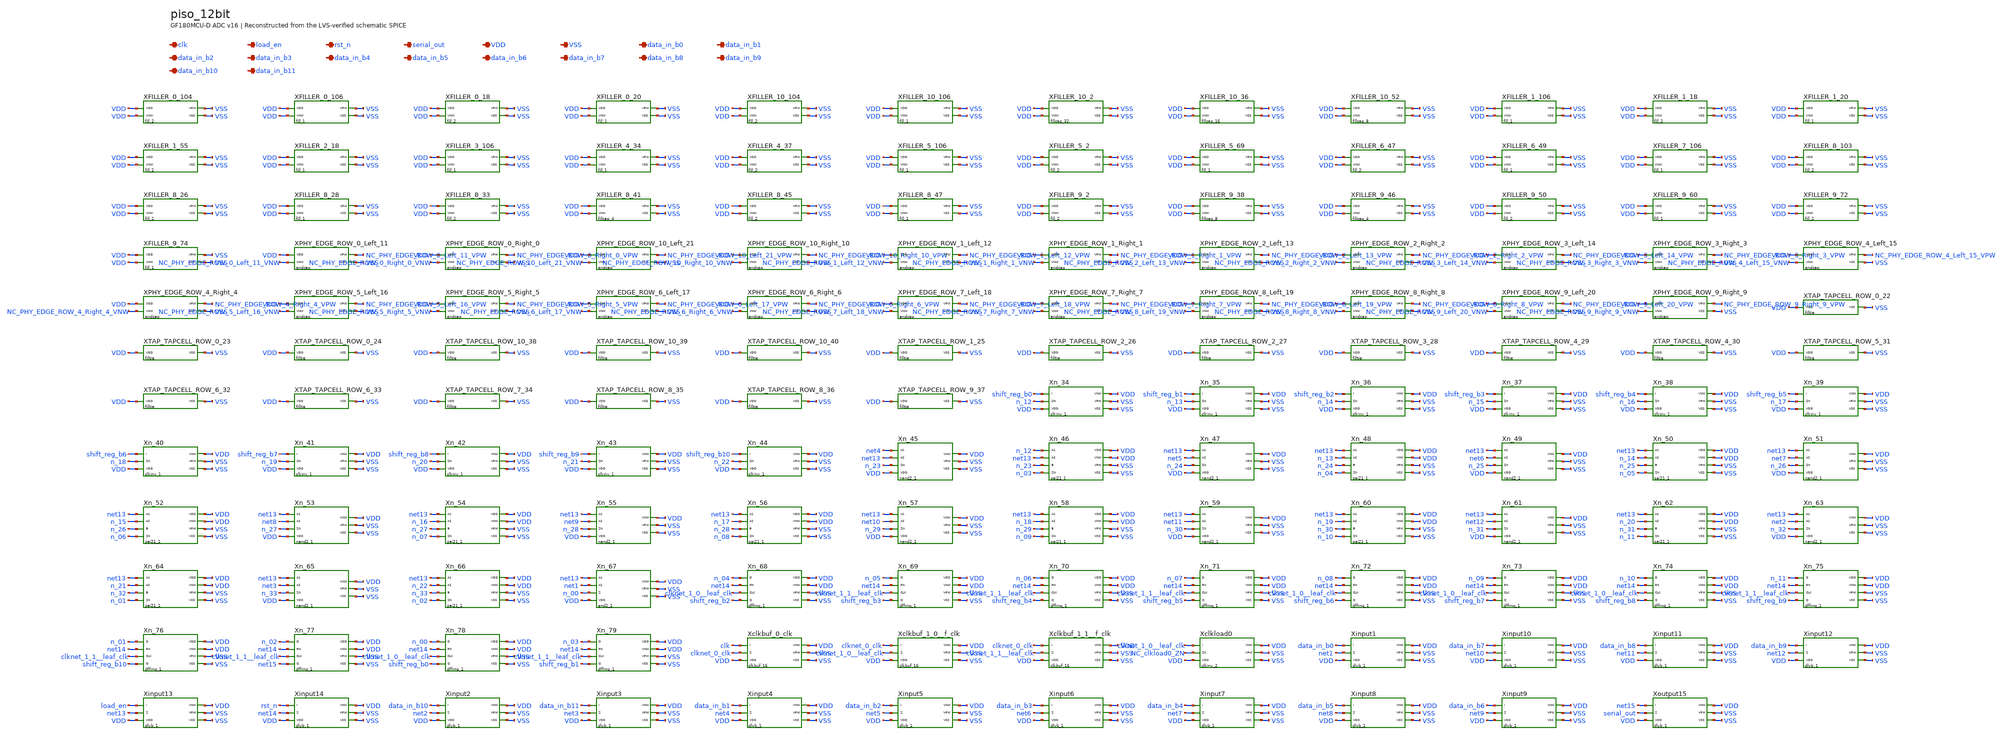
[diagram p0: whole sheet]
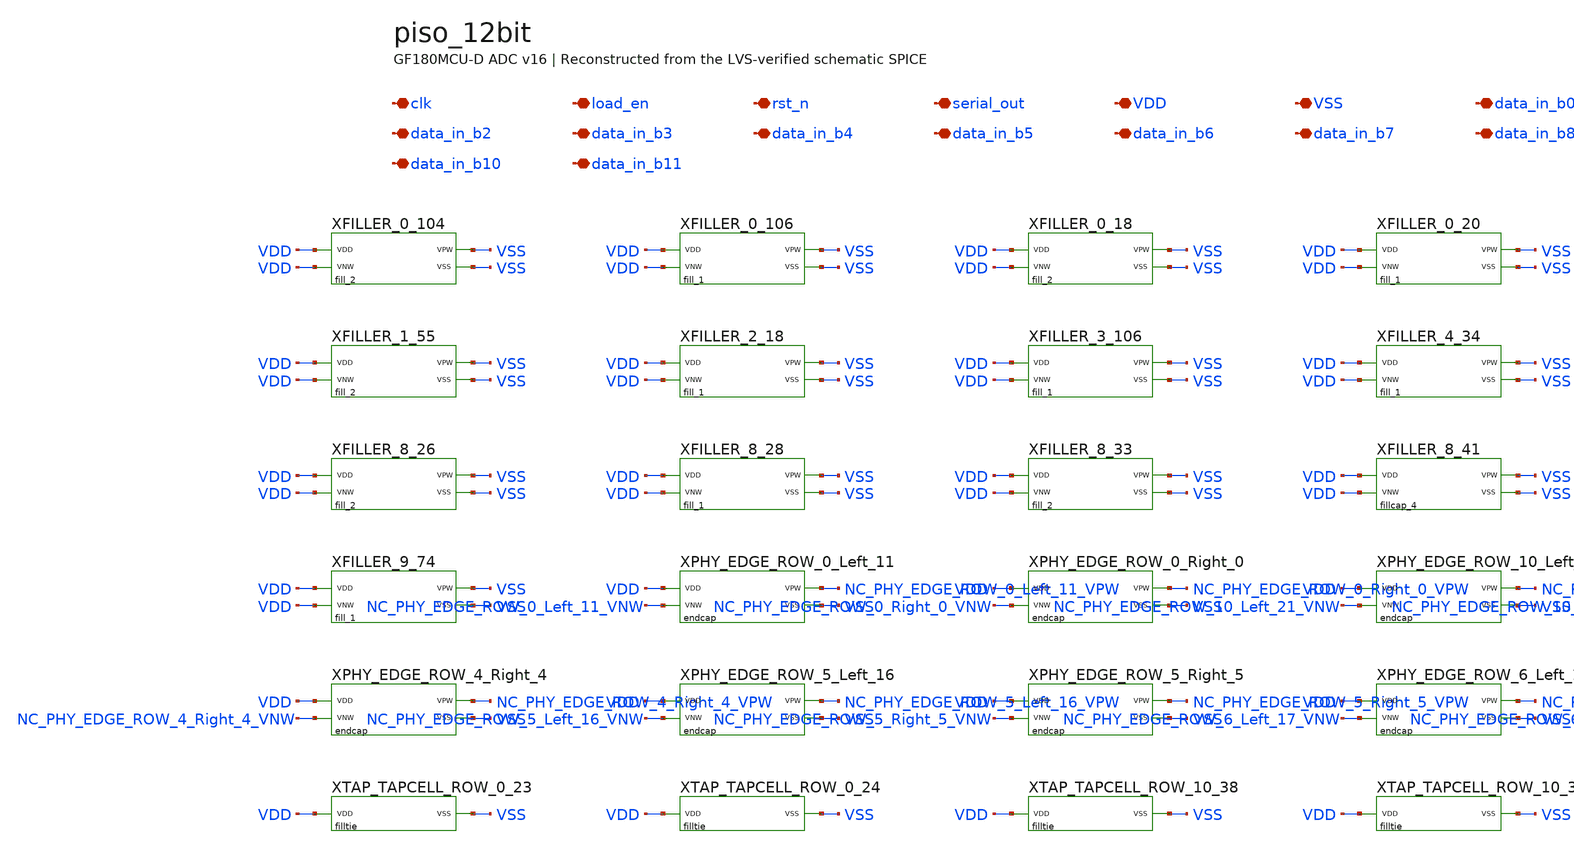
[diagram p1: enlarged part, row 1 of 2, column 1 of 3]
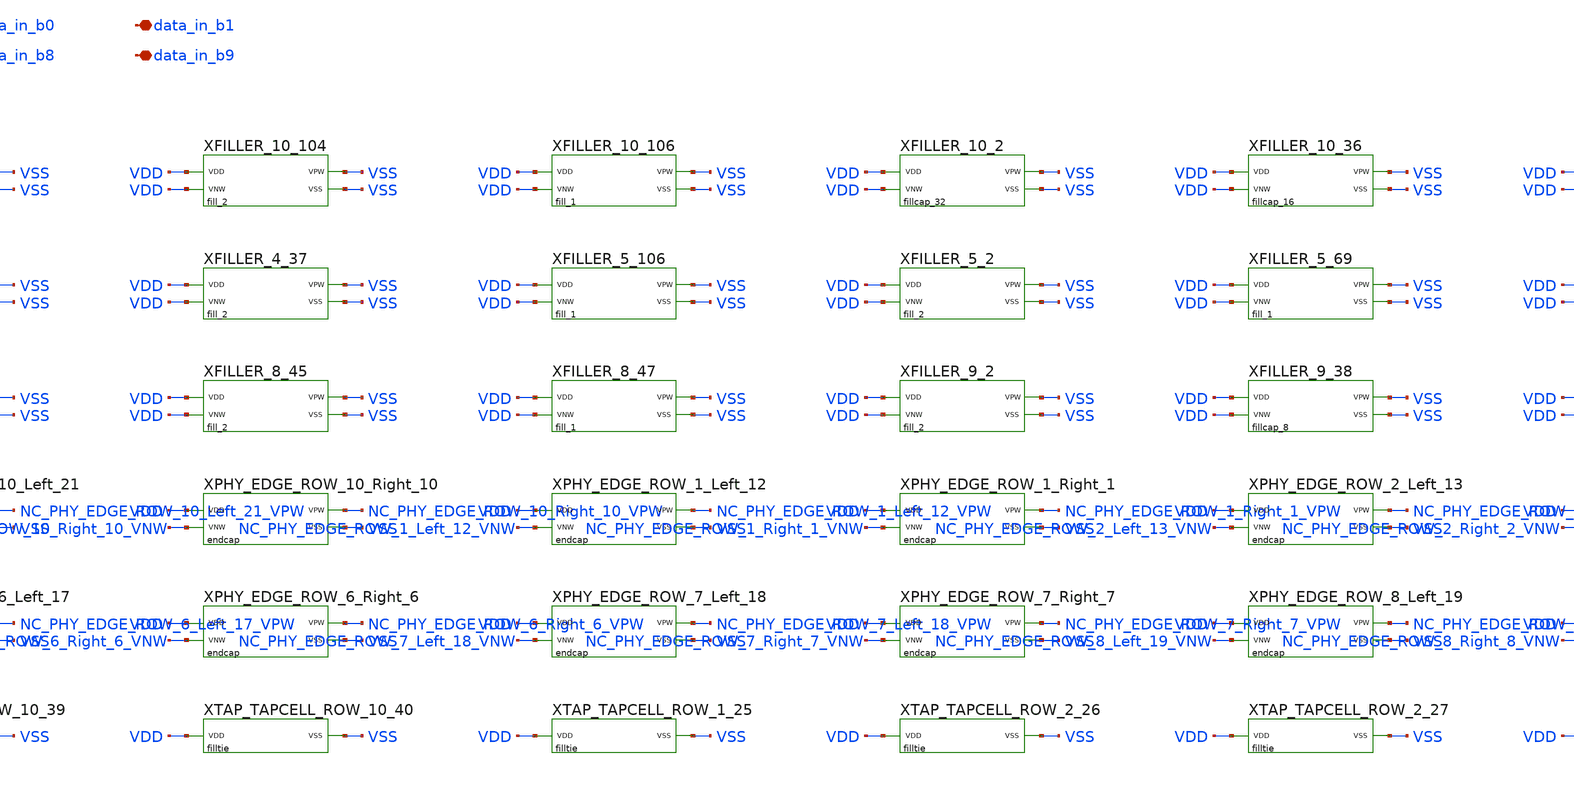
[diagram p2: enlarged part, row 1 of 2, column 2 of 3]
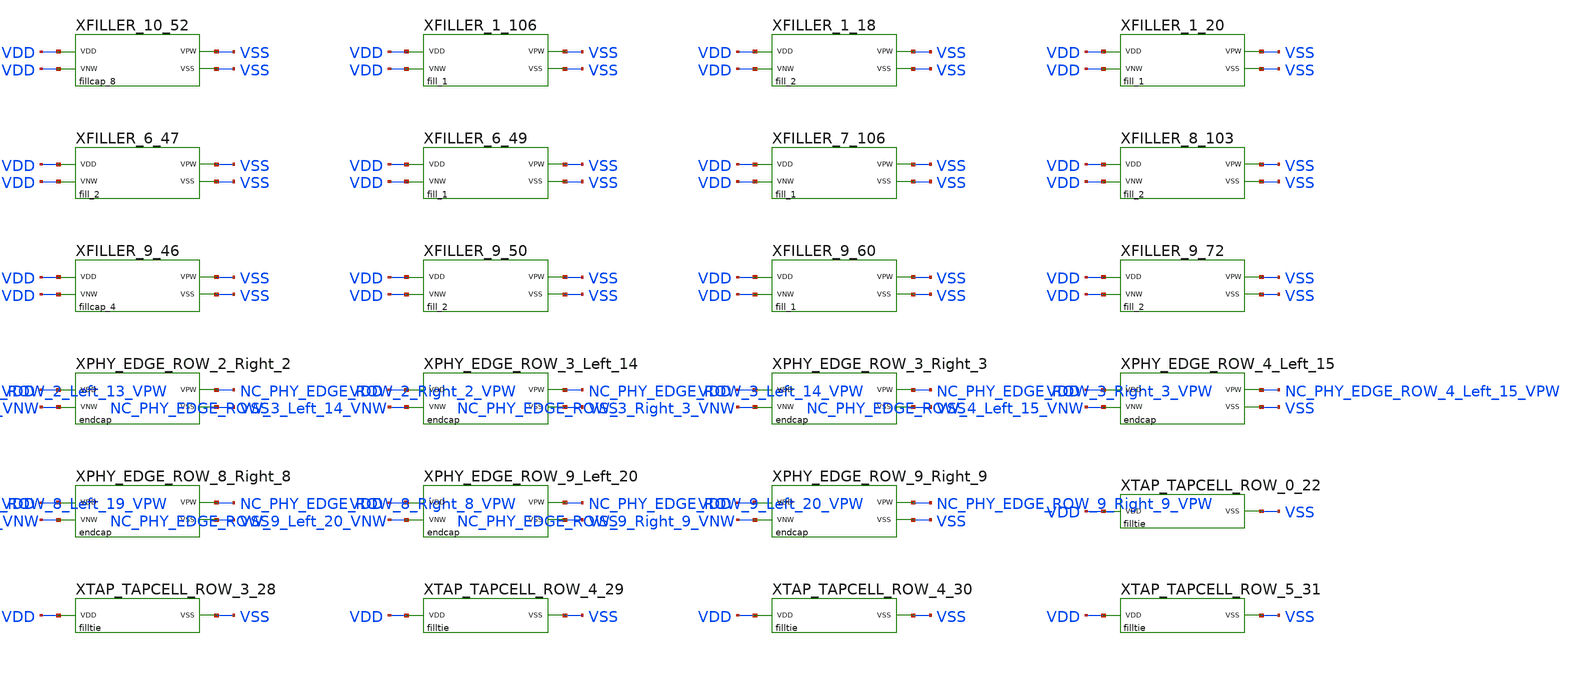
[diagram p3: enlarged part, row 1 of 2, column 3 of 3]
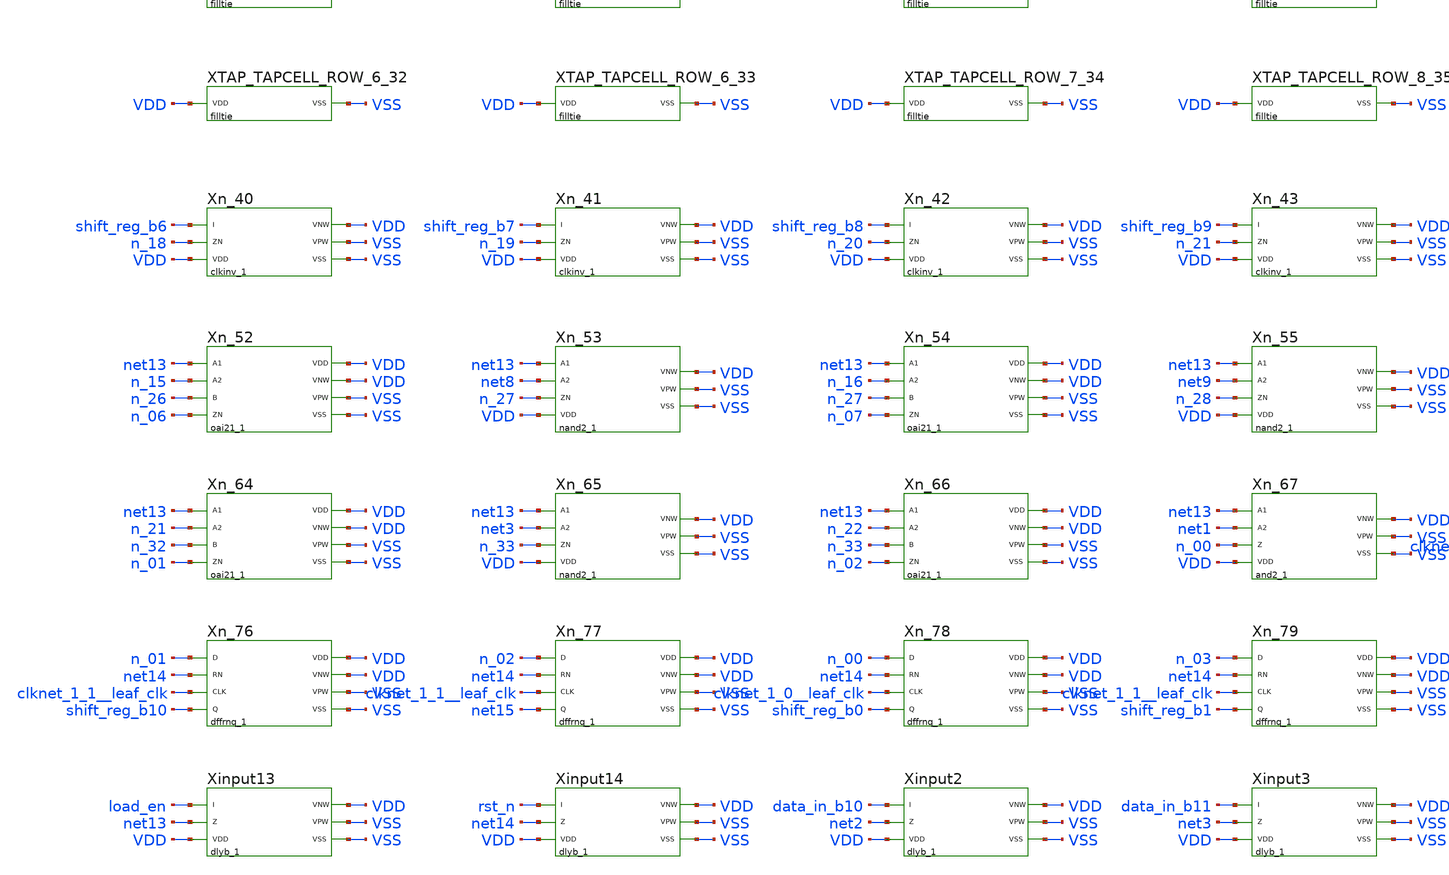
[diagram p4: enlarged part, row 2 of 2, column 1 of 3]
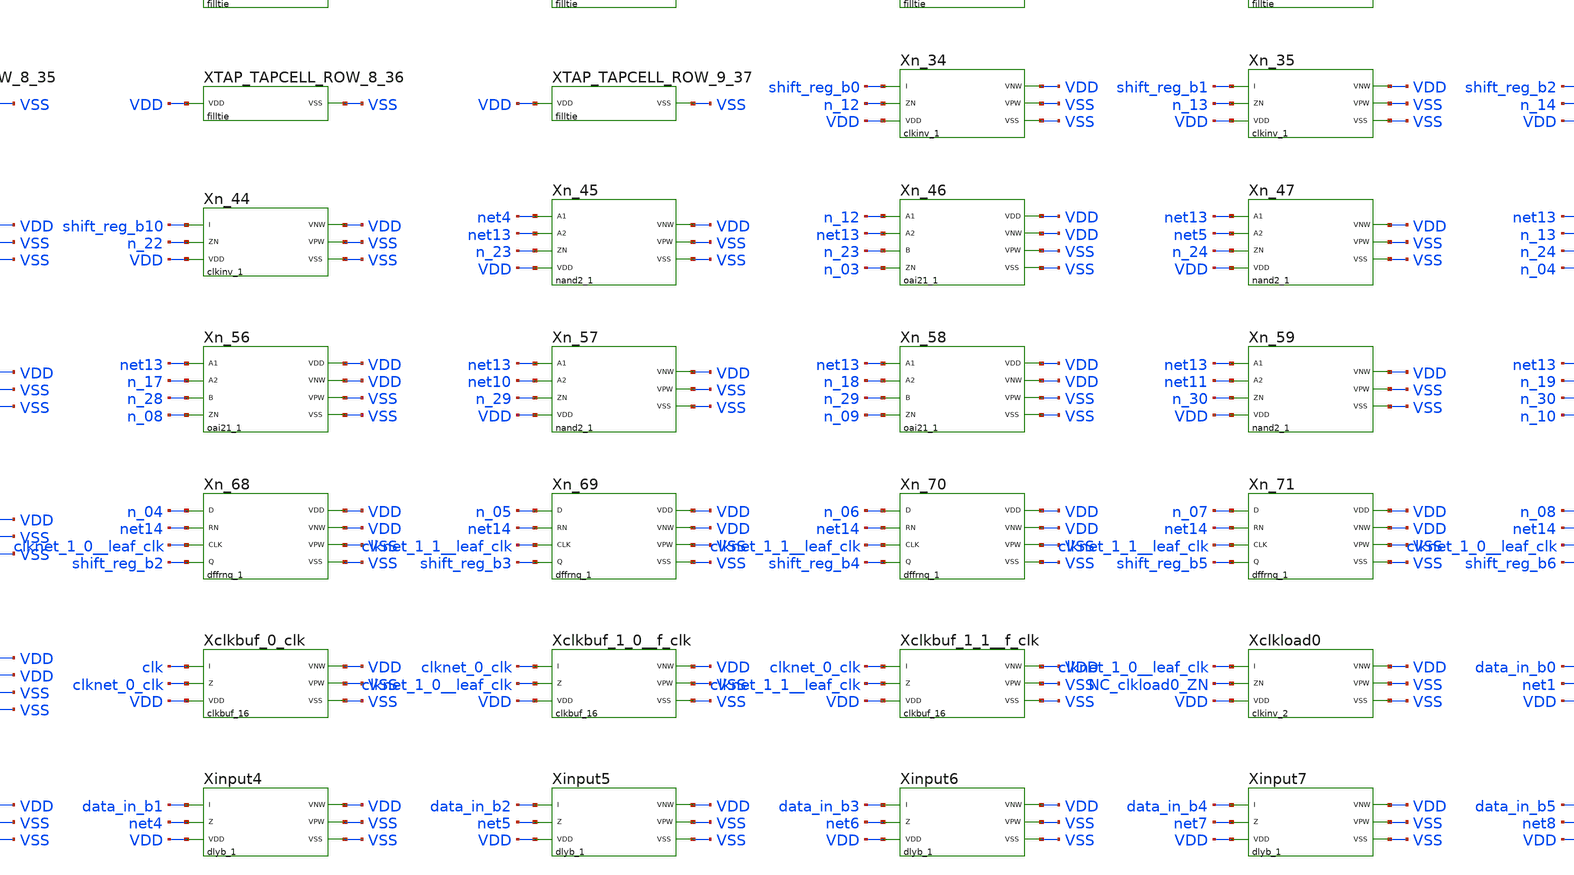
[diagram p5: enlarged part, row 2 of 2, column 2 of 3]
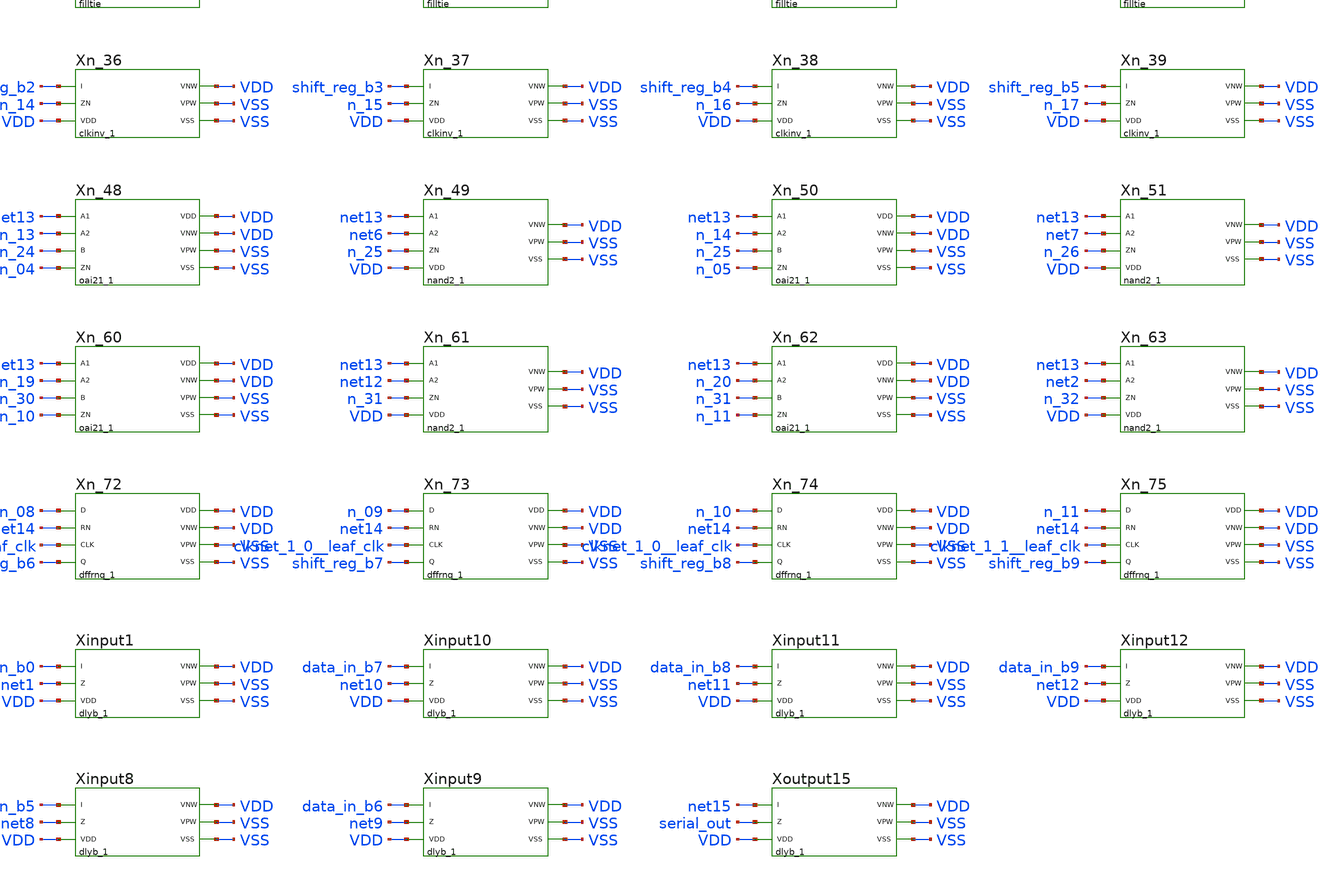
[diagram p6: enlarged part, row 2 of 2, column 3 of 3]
** sch_path: src/schematics/INTEGRATION/ADC_final/ADC_v17_Xschem/piso_12bit.sch
* Copyright (C) 1998-2026 Stefan Frederik Schippers
* This program is free software; you can redistribute it and/or modify
* it under the terms of the GNU General Public License as published by
* the Free Software Foundation; either version 2 of the License, or
* (at your option) any later version.
**.subckt piso_12bit clk load_en rst_n serial_out VDD VSS data_in_b0 data_in_b1 data_in_b2
*+ data_in_b3 data_in_b4 data_in_b5 data_in_b6 data_in_b7 data_in_b8 data_in_b9 data_in_b10 data_in_b11
*.iopin clk
*.iopin load_en
*.iopin rst_n
*.iopin serial_out
*.iopin VDD
*.iopin VSS
*.iopin data_in_b0
*.iopin data_in_b1
*.iopin data_in_b2
*.iopin data_in_b3
*.iopin data_in_b4
*.iopin data_in_b5
*.iopin data_in_b6
*.iopin data_in_b7
*.iopin data_in_b8
*.iopin data_in_b9
*.iopin data_in_b10
*.iopin data_in_b11
XFILLER_0_104 VDD VDD VSS VSS gf180mcu_fd_sc_mcu7t5v0__fill_2
XFILLER_0_106 VDD VDD VSS VSS gf180mcu_fd_sc_mcu7t5v0__fill_1
XFILLER_0_18 VDD VDD VSS VSS gf180mcu_fd_sc_mcu7t5v0__fill_2
XFILLER_0_20 VDD VDD VSS VSS gf180mcu_fd_sc_mcu7t5v0__fill_1
XFILLER_10_104 VDD VDD VSS VSS gf180mcu_fd_sc_mcu7t5v0__fill_2
XFILLER_10_106 VDD VDD VSS VSS gf180mcu_fd_sc_mcu7t5v0__fill_1
XFILLER_10_2 VDD VDD VSS VSS gf180mcu_fd_sc_mcu7t5v0__fillcap_32
XFILLER_10_36 VDD VDD VSS VSS gf180mcu_fd_sc_mcu7t5v0__fillcap_16
XFILLER_10_52 VDD VDD VSS VSS gf180mcu_fd_sc_mcu7t5v0__fillcap_8
XFILLER_1_106 VDD VDD VSS VSS gf180mcu_fd_sc_mcu7t5v0__fill_1
XFILLER_1_18 VDD VDD VSS VSS gf180mcu_fd_sc_mcu7t5v0__fill_2
XFILLER_1_20 VDD VDD VSS VSS gf180mcu_fd_sc_mcu7t5v0__fill_1
XFILLER_1_55 VDD VDD VSS VSS gf180mcu_fd_sc_mcu7t5v0__fill_2
XFILLER_2_18 VDD VDD VSS VSS gf180mcu_fd_sc_mcu7t5v0__fill_1
XFILLER_3_106 VDD VDD VSS VSS gf180mcu_fd_sc_mcu7t5v0__fill_1
XFILLER_4_34 VDD VDD VSS VSS gf180mcu_fd_sc_mcu7t5v0__fill_1
XFILLER_4_37 VDD VDD VSS VSS gf180mcu_fd_sc_mcu7t5v0__fill_2
XFILLER_5_106 VDD VDD VSS VSS gf180mcu_fd_sc_mcu7t5v0__fill_1
XFILLER_5_2 VDD VDD VSS VSS gf180mcu_fd_sc_mcu7t5v0__fill_2
XFILLER_5_69 VDD VDD VSS VSS gf180mcu_fd_sc_mcu7t5v0__fill_1
XFILLER_6_47 VDD VDD VSS VSS gf180mcu_fd_sc_mcu7t5v0__fill_2
XFILLER_6_49 VDD VDD VSS VSS gf180mcu_fd_sc_mcu7t5v0__fill_1
XFILLER_7_106 VDD VDD VSS VSS gf180mcu_fd_sc_mcu7t5v0__fill_1
XFILLER_8_103 VDD VDD VSS VSS gf180mcu_fd_sc_mcu7t5v0__fill_2
XFILLER_8_26 VDD VDD VSS VSS gf180mcu_fd_sc_mcu7t5v0__fill_2
XFILLER_8_28 VDD VDD VSS VSS gf180mcu_fd_sc_mcu7t5v0__fill_1
XFILLER_8_33 VDD VDD VSS VSS gf180mcu_fd_sc_mcu7t5v0__fill_2
XFILLER_8_41 VDD VDD VSS VSS gf180mcu_fd_sc_mcu7t5v0__fillcap_4
XFILLER_8_45 VDD VDD VSS VSS gf180mcu_fd_sc_mcu7t5v0__fill_2
XFILLER_8_47 VDD VDD VSS VSS gf180mcu_fd_sc_mcu7t5v0__fill_1
XFILLER_9_2 VDD VDD VSS VSS gf180mcu_fd_sc_mcu7t5v0__fill_2
XFILLER_9_38 VDD VDD VSS VSS gf180mcu_fd_sc_mcu7t5v0__fillcap_8
XFILLER_9_46 VDD VDD VSS VSS gf180mcu_fd_sc_mcu7t5v0__fillcap_4
XFILLER_9_50 VDD VDD VSS VSS gf180mcu_fd_sc_mcu7t5v0__fill_2
XFILLER_9_60 VDD VDD VSS VSS gf180mcu_fd_sc_mcu7t5v0__fill_1
XFILLER_9_72 VDD VDD VSS VSS gf180mcu_fd_sc_mcu7t5v0__fill_2
XFILLER_9_74 VDD VDD VSS VSS gf180mcu_fd_sc_mcu7t5v0__fill_1
XPHY_EDGE_ROW_0_Left_11 VDD NC_PHY_EDGE_ROW_0_Left_11_VNW NC_PHY_EDGE_ROW_0_Left_11_VPW VSS
+ gf180mcu_fd_sc_mcu7t5v0__endcap
XPHY_EDGE_ROW_0_Right_0 VDD NC_PHY_EDGE_ROW_0_Right_0_VNW NC_PHY_EDGE_ROW_0_Right_0_VPW VSS
+ gf180mcu_fd_sc_mcu7t5v0__endcap
XPHY_EDGE_ROW_10_Left_21 VDD NC_PHY_EDGE_ROW_10_Left_21_VNW NC_PHY_EDGE_ROW_10_Left_21_VPW VSS
+ gf180mcu_fd_sc_mcu7t5v0__endcap
XPHY_EDGE_ROW_10_Right_10 VDD NC_PHY_EDGE_ROW_10_Right_10_VNW NC_PHY_EDGE_ROW_10_Right_10_VPW VSS
+ gf180mcu_fd_sc_mcu7t5v0__endcap
XPHY_EDGE_ROW_1_Left_12 VDD NC_PHY_EDGE_ROW_1_Left_12_VNW NC_PHY_EDGE_ROW_1_Left_12_VPW VSS
+ gf180mcu_fd_sc_mcu7t5v0__endcap
XPHY_EDGE_ROW_1_Right_1 VDD NC_PHY_EDGE_ROW_1_Right_1_VNW NC_PHY_EDGE_ROW_1_Right_1_VPW VSS
+ gf180mcu_fd_sc_mcu7t5v0__endcap
XPHY_EDGE_ROW_2_Left_13 VDD NC_PHY_EDGE_ROW_2_Left_13_VNW NC_PHY_EDGE_ROW_2_Left_13_VPW VSS
+ gf180mcu_fd_sc_mcu7t5v0__endcap
XPHY_EDGE_ROW_2_Right_2 VDD NC_PHY_EDGE_ROW_2_Right_2_VNW NC_PHY_EDGE_ROW_2_Right_2_VPW VSS
+ gf180mcu_fd_sc_mcu7t5v0__endcap
XPHY_EDGE_ROW_3_Left_14 VDD NC_PHY_EDGE_ROW_3_Left_14_VNW NC_PHY_EDGE_ROW_3_Left_14_VPW VSS
+ gf180mcu_fd_sc_mcu7t5v0__endcap
XPHY_EDGE_ROW_3_Right_3 VDD NC_PHY_EDGE_ROW_3_Right_3_VNW NC_PHY_EDGE_ROW_3_Right_3_VPW VSS
+ gf180mcu_fd_sc_mcu7t5v0__endcap
XPHY_EDGE_ROW_4_Left_15 VDD NC_PHY_EDGE_ROW_4_Left_15_VNW NC_PHY_EDGE_ROW_4_Left_15_VPW VSS
+ gf180mcu_fd_sc_mcu7t5v0__endcap
XPHY_EDGE_ROW_4_Right_4 VDD NC_PHY_EDGE_ROW_4_Right_4_VNW NC_PHY_EDGE_ROW_4_Right_4_VPW VSS
+ gf180mcu_fd_sc_mcu7t5v0__endcap
XPHY_EDGE_ROW_5_Left_16 VDD NC_PHY_EDGE_ROW_5_Left_16_VNW NC_PHY_EDGE_ROW_5_Left_16_VPW VSS
+ gf180mcu_fd_sc_mcu7t5v0__endcap
XPHY_EDGE_ROW_5_Right_5 VDD NC_PHY_EDGE_ROW_5_Right_5_VNW NC_PHY_EDGE_ROW_5_Right_5_VPW VSS
+ gf180mcu_fd_sc_mcu7t5v0__endcap
XPHY_EDGE_ROW_6_Left_17 VDD NC_PHY_EDGE_ROW_6_Left_17_VNW NC_PHY_EDGE_ROW_6_Left_17_VPW VSS
+ gf180mcu_fd_sc_mcu7t5v0__endcap
XPHY_EDGE_ROW_6_Right_6 VDD NC_PHY_EDGE_ROW_6_Right_6_VNW NC_PHY_EDGE_ROW_6_Right_6_VPW VSS
+ gf180mcu_fd_sc_mcu7t5v0__endcap
XPHY_EDGE_ROW_7_Left_18 VDD NC_PHY_EDGE_ROW_7_Left_18_VNW NC_PHY_EDGE_ROW_7_Left_18_VPW VSS
+ gf180mcu_fd_sc_mcu7t5v0__endcap
XPHY_EDGE_ROW_7_Right_7 VDD NC_PHY_EDGE_ROW_7_Right_7_VNW NC_PHY_EDGE_ROW_7_Right_7_VPW VSS
+ gf180mcu_fd_sc_mcu7t5v0__endcap
XPHY_EDGE_ROW_8_Left_19 VDD NC_PHY_EDGE_ROW_8_Left_19_VNW NC_PHY_EDGE_ROW_8_Left_19_VPW VSS
+ gf180mcu_fd_sc_mcu7t5v0__endcap
XPHY_EDGE_ROW_8_Right_8 VDD NC_PHY_EDGE_ROW_8_Right_8_VNW NC_PHY_EDGE_ROW_8_Right_8_VPW VSS
+ gf180mcu_fd_sc_mcu7t5v0__endcap
XPHY_EDGE_ROW_9_Left_20 VDD NC_PHY_EDGE_ROW_9_Left_20_VNW NC_PHY_EDGE_ROW_9_Left_20_VPW VSS
+ gf180mcu_fd_sc_mcu7t5v0__endcap
XPHY_EDGE_ROW_9_Right_9 VDD NC_PHY_EDGE_ROW_9_Right_9_VNW NC_PHY_EDGE_ROW_9_Right_9_VPW VSS
+ gf180mcu_fd_sc_mcu7t5v0__endcap
XTAP_TAPCELL_ROW_0_22 VDD VSS gf180mcu_fd_sc_mcu7t5v0__filltie
XTAP_TAPCELL_ROW_0_23 VDD VSS gf180mcu_fd_sc_mcu7t5v0__filltie
XTAP_TAPCELL_ROW_0_24 VDD VSS gf180mcu_fd_sc_mcu7t5v0__filltie
XTAP_TAPCELL_ROW_10_38 VDD VSS gf180mcu_fd_sc_mcu7t5v0__filltie
XTAP_TAPCELL_ROW_10_39 VDD VSS gf180mcu_fd_sc_mcu7t5v0__filltie
XTAP_TAPCELL_ROW_10_40 VDD VSS gf180mcu_fd_sc_mcu7t5v0__filltie
XTAP_TAPCELL_ROW_1_25 VDD VSS gf180mcu_fd_sc_mcu7t5v0__filltie
XTAP_TAPCELL_ROW_2_26 VDD VSS gf180mcu_fd_sc_mcu7t5v0__filltie
XTAP_TAPCELL_ROW_2_27 VDD VSS gf180mcu_fd_sc_mcu7t5v0__filltie
XTAP_TAPCELL_ROW_3_28 VDD VSS gf180mcu_fd_sc_mcu7t5v0__filltie
XTAP_TAPCELL_ROW_4_29 VDD VSS gf180mcu_fd_sc_mcu7t5v0__filltie
XTAP_TAPCELL_ROW_4_30 VDD VSS gf180mcu_fd_sc_mcu7t5v0__filltie
XTAP_TAPCELL_ROW_5_31 VDD VSS gf180mcu_fd_sc_mcu7t5v0__filltie
XTAP_TAPCELL_ROW_6_32 VDD VSS gf180mcu_fd_sc_mcu7t5v0__filltie
XTAP_TAPCELL_ROW_6_33 VDD VSS gf180mcu_fd_sc_mcu7t5v0__filltie
XTAP_TAPCELL_ROW_7_34 VDD VSS gf180mcu_fd_sc_mcu7t5v0__filltie
XTAP_TAPCELL_ROW_8_35 VDD VSS gf180mcu_fd_sc_mcu7t5v0__filltie
XTAP_TAPCELL_ROW_8_36 VDD VSS gf180mcu_fd_sc_mcu7t5v0__filltie
XTAP_TAPCELL_ROW_9_37 VDD VSS gf180mcu_fd_sc_mcu7t5v0__filltie
Xn_34 shift_reg_b0 n_12 VDD VDD VSS VSS gf180mcu_fd_sc_mcu7t5v0__clkinv_1
Xn_35 shift_reg_b1 n_13 VDD VDD VSS VSS gf180mcu_fd_sc_mcu7t5v0__clkinv_1
Xn_36 shift_reg_b2 n_14 VDD VDD VSS VSS gf180mcu_fd_sc_mcu7t5v0__clkinv_1
Xn_37 shift_reg_b3 n_15 VDD VDD VSS VSS gf180mcu_fd_sc_mcu7t5v0__clkinv_1
Xn_38 shift_reg_b4 n_16 VDD VDD VSS VSS gf180mcu_fd_sc_mcu7t5v0__clkinv_1
Xn_39 shift_reg_b5 n_17 VDD VDD VSS VSS gf180mcu_fd_sc_mcu7t5v0__clkinv_1
Xn_40 shift_reg_b6 n_18 VDD VDD VSS VSS gf180mcu_fd_sc_mcu7t5v0__clkinv_1
Xn_41 shift_reg_b7 n_19 VDD VDD VSS VSS gf180mcu_fd_sc_mcu7t5v0__clkinv_1
Xn_42 shift_reg_b8 n_20 VDD VDD VSS VSS gf180mcu_fd_sc_mcu7t5v0__clkinv_1
Xn_43 shift_reg_b9 n_21 VDD VDD VSS VSS gf180mcu_fd_sc_mcu7t5v0__clkinv_1
Xn_44 shift_reg_b10 n_22 VDD VDD VSS VSS gf180mcu_fd_sc_mcu7t5v0__clkinv_1
Xn_45 net4 net13 n_23 VDD VDD VSS VSS gf180mcu_fd_sc_mcu7t5v0__nand2_1
Xn_46 n_12 net13 n_23 n_03 VDD VDD VSS VSS gf180mcu_fd_sc_mcu7t5v0__oai21_1
Xn_47 net13 net5 n_24 VDD VDD VSS VSS gf180mcu_fd_sc_mcu7t5v0__nand2_1
Xn_48 net13 n_13 n_24 n_04 VDD VDD VSS VSS gf180mcu_fd_sc_mcu7t5v0__oai21_1
Xn_49 net13 net6 n_25 VDD VDD VSS VSS gf180mcu_fd_sc_mcu7t5v0__nand2_1
Xn_50 net13 n_14 n_25 n_05 VDD VDD VSS VSS gf180mcu_fd_sc_mcu7t5v0__oai21_1
Xn_51 net13 net7 n_26 VDD VDD VSS VSS gf180mcu_fd_sc_mcu7t5v0__nand2_1
Xn_52 net13 n_15 n_26 n_06 VDD VDD VSS VSS gf180mcu_fd_sc_mcu7t5v0__oai21_1
Xn_53 net13 net8 n_27 VDD VDD VSS VSS gf180mcu_fd_sc_mcu7t5v0__nand2_1
Xn_54 net13 n_16 n_27 n_07 VDD VDD VSS VSS gf180mcu_fd_sc_mcu7t5v0__oai21_1
Xn_55 net13 net9 n_28 VDD VDD VSS VSS gf180mcu_fd_sc_mcu7t5v0__nand2_1
Xn_56 net13 n_17 n_28 n_08 VDD VDD VSS VSS gf180mcu_fd_sc_mcu7t5v0__oai21_1
Xn_57 net13 net10 n_29 VDD VDD VSS VSS gf180mcu_fd_sc_mcu7t5v0__nand2_1
Xn_58 net13 n_18 n_29 n_09 VDD VDD VSS VSS gf180mcu_fd_sc_mcu7t5v0__oai21_1
Xn_59 net13 net11 n_30 VDD VDD VSS VSS gf180mcu_fd_sc_mcu7t5v0__nand2_1
Xn_60 net13 n_19 n_30 n_10 VDD VDD VSS VSS gf180mcu_fd_sc_mcu7t5v0__oai21_1
Xn_61 net13 net12 n_31 VDD VDD VSS VSS gf180mcu_fd_sc_mcu7t5v0__nand2_1
Xn_62 net13 n_20 n_31 n_11 VDD VDD VSS VSS gf180mcu_fd_sc_mcu7t5v0__oai21_1
Xn_63 net13 net2 n_32 VDD VDD VSS VSS gf180mcu_fd_sc_mcu7t5v0__nand2_1
Xn_64 net13 n_21 n_32 n_01 VDD VDD VSS VSS gf180mcu_fd_sc_mcu7t5v0__oai21_1
Xn_65 net13 net3 n_33 VDD VDD VSS VSS gf180mcu_fd_sc_mcu7t5v0__nand2_1
Xn_66 net13 n_22 n_33 n_02 VDD VDD VSS VSS gf180mcu_fd_sc_mcu7t5v0__oai21_1
Xn_67 net13 net1 n_00 VDD VDD VSS VSS gf180mcu_fd_sc_mcu7t5v0__and2_1
Xn_68 n_04 net14 clknet_1_0__leaf_clk shift_reg_b2 VDD VDD VSS VSS gf180mcu_fd_sc_mcu7t5v0__dffrnq_1
Xn_69 n_05 net14 clknet_1_1__leaf_clk shift_reg_b3 VDD VDD VSS VSS gf180mcu_fd_sc_mcu7t5v0__dffrnq_1
Xn_70 n_06 net14 clknet_1_1__leaf_clk shift_reg_b4 VDD VDD VSS VSS gf180mcu_fd_sc_mcu7t5v0__dffrnq_1
Xn_71 n_07 net14 clknet_1_1__leaf_clk shift_reg_b5 VDD VDD VSS VSS gf180mcu_fd_sc_mcu7t5v0__dffrnq_1
Xn_72 n_08 net14 clknet_1_0__leaf_clk shift_reg_b6 VDD VDD VSS VSS gf180mcu_fd_sc_mcu7t5v0__dffrnq_1
Xn_73 n_09 net14 clknet_1_0__leaf_clk shift_reg_b7 VDD VDD VSS VSS gf180mcu_fd_sc_mcu7t5v0__dffrnq_1
Xn_74 n_10 net14 clknet_1_0__leaf_clk shift_reg_b8 VDD VDD VSS VSS gf180mcu_fd_sc_mcu7t5v0__dffrnq_1
Xn_75 n_11 net14 clknet_1_1__leaf_clk shift_reg_b9 VDD VDD VSS VSS gf180mcu_fd_sc_mcu7t5v0__dffrnq_1
Xn_76 n_01 net14 clknet_1_1__leaf_clk shift_reg_b10 VDD VDD VSS VSS
+ gf180mcu_fd_sc_mcu7t5v0__dffrnq_1
Xn_77 n_02 net14 clknet_1_1__leaf_clk net15 VDD VDD VSS VSS gf180mcu_fd_sc_mcu7t5v0__dffrnq_1
Xn_78 n_00 net14 clknet_1_0__leaf_clk shift_reg_b0 VDD VDD VSS VSS gf180mcu_fd_sc_mcu7t5v0__dffrnq_1
Xn_79 n_03 net14 clknet_1_1__leaf_clk shift_reg_b1 VDD VDD VSS VSS gf180mcu_fd_sc_mcu7t5v0__dffrnq_1
Xclkbuf_0_clk clk clknet_0_clk VDD VDD VSS VSS gf180mcu_fd_sc_mcu7t5v0__clkbuf_16
Xclkbuf_1_0__f_clk clknet_0_clk clknet_1_0__leaf_clk VDD VDD VSS VSS
+ gf180mcu_fd_sc_mcu7t5v0__clkbuf_16
Xclkbuf_1_1__f_clk clknet_0_clk clknet_1_1__leaf_clk VDD VDD VSS VSS
+ gf180mcu_fd_sc_mcu7t5v0__clkbuf_16
Xclkload0 clknet_1_0__leaf_clk NC_clkload0_ZN VDD VDD VSS VSS gf180mcu_fd_sc_mcu7t5v0__clkinv_2
Xinput1 data_in_b0 net1 VDD VDD VSS VSS gf180mcu_fd_sc_mcu7t5v0__dlyb_1
Xinput10 data_in_b7 net10 VDD VDD VSS VSS gf180mcu_fd_sc_mcu7t5v0__dlyb_1
Xinput11 data_in_b8 net11 VDD VDD VSS VSS gf180mcu_fd_sc_mcu7t5v0__dlyb_1
Xinput12 data_in_b9 net12 VDD VDD VSS VSS gf180mcu_fd_sc_mcu7t5v0__dlyb_1
Xinput13 load_en net13 VDD VDD VSS VSS gf180mcu_fd_sc_mcu7t5v0__dlyb_1
Xinput14 rst_n net14 VDD VDD VSS VSS gf180mcu_fd_sc_mcu7t5v0__dlyb_1
Xinput2 data_in_b10 net2 VDD VDD VSS VSS gf180mcu_fd_sc_mcu7t5v0__dlyb_1
Xinput3 data_in_b11 net3 VDD VDD VSS VSS gf180mcu_fd_sc_mcu7t5v0__dlyb_1
Xinput4 data_in_b1 net4 VDD VDD VSS VSS gf180mcu_fd_sc_mcu7t5v0__dlyb_1
Xinput5 data_in_b2 net5 VDD VDD VSS VSS gf180mcu_fd_sc_mcu7t5v0__dlyb_1
Xinput6 data_in_b3 net6 VDD VDD VSS VSS gf180mcu_fd_sc_mcu7t5v0__dlyb_1
Xinput7 data_in_b4 net7 VDD VDD VSS VSS gf180mcu_fd_sc_mcu7t5v0__dlyb_1
Xinput8 data_in_b5 net8 VDD VDD VSS VSS gf180mcu_fd_sc_mcu7t5v0__dlyb_1
Xinput9 data_in_b6 net9 VDD VDD VSS VSS gf180mcu_fd_sc_mcu7t5v0__dlyb_1
Xoutput15 net15 serial_out VDD VDD VSS VSS gf180mcu_fd_sc_mcu7t5v0__dlyb_1
**.ends
.end
